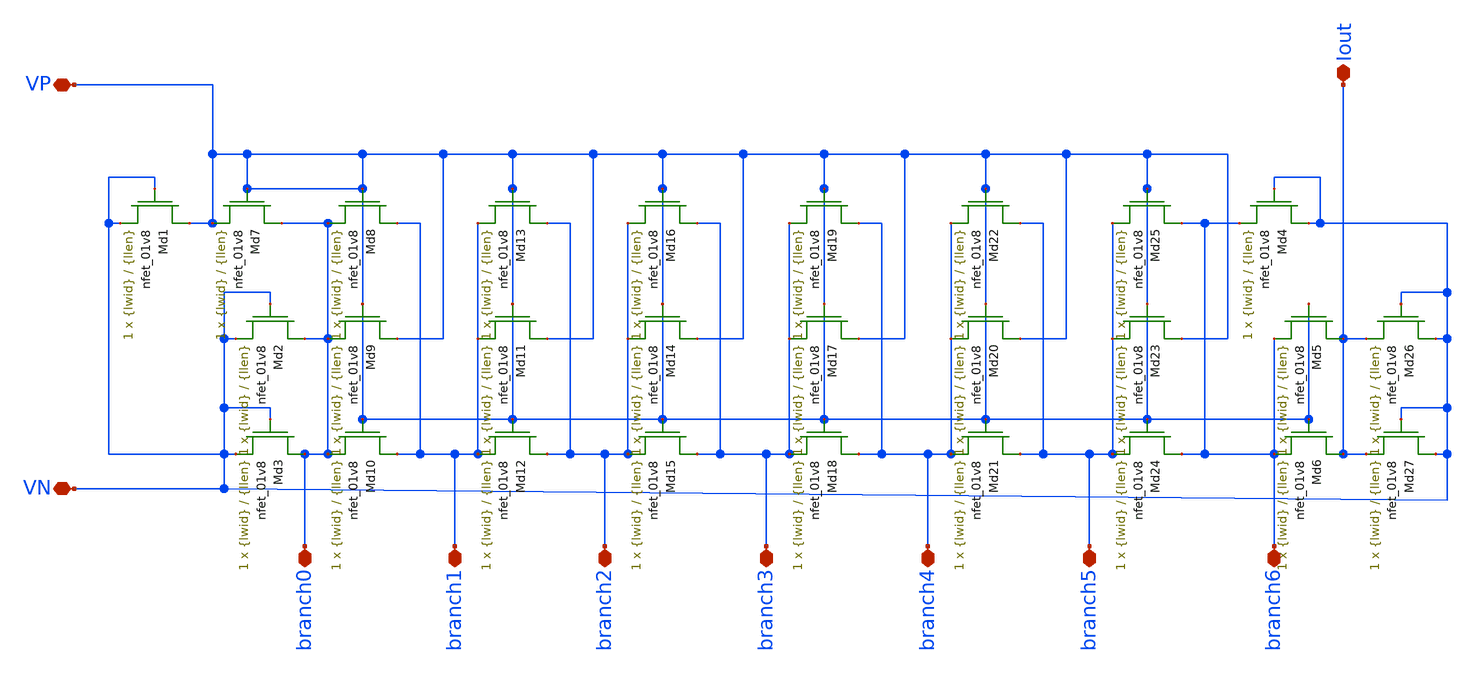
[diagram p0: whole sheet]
** sch_path: design-files/improved/dacladder-m2.sch
**.subckt dacladder-m2 branch0 branch1 branch2 branch3 branch4 branch5 branch6 Iout VN VP
*.iopin branch0
*.iopin branch1
*.iopin branch2
*.iopin branch3
*.iopin branch4
*.iopin branch5
*.iopin branch6
*.iopin Iout
*.iopin VN
*.iopin VP
XMd1 VP VN VN GND sky130_fd_pr__nfet_01v8 L={llen} W={lwid} nf=1 ad='int((nf+1)/2) * W/nf * 0.29' as='int((nf+2)/2) * W/nf * 0.29'
+ pd='2*int((nf+1)/2) * (W/nf + 0.29)' ps='2*int((nf+2)/2) * (W/nf + 0.29)' nrd='0.29 / W' nrs='0.29 / W'
+ sa=0 sb=0 sd=0 mult=1 m=1
XMd7 branch0 VP VP GND sky130_fd_pr__nfet_01v8 L={llen} W={lwid} nf=1 ad='int((nf+1)/2) * W/nf * 0.29'
+ as='int((nf+2)/2) * W/nf * 0.29' pd='2*int((nf+1)/2) * (W/nf + 0.29)' ps='2*int((nf+2)/2) * (W/nf + 0.29)'
+ nrd='0.29 / W' nrs='0.29 / W' sa=0 sb=0 sd=0 mult=1 m=1
XMd8 branch1 VP branch0 GND sky130_fd_pr__nfet_01v8 L={llen} W={lwid} nf=1 ad='int((nf+1)/2) * W/nf * 0.29'
+ as='int((nf+2)/2) * W/nf * 0.29' pd='2*int((nf+1)/2) * (W/nf + 0.29)' ps='2*int((nf+2)/2) * (W/nf + 0.29)'
+ nrd='0.29 / W' nrs='0.29 / W' sa=0 sb=0 sd=0 mult=1 m=1
XMd2 branch0 VN VN GND sky130_fd_pr__nfet_01v8 L={llen} W={lwid} nf=1 ad='int((nf+1)/2) * W/nf * 0.29'
+ as='int((nf+2)/2) * W/nf * 0.29' pd='2*int((nf+1)/2) * (W/nf + 0.29)' ps='2*int((nf+2)/2) * (W/nf + 0.29)'
+ nrd='0.29 / W' nrs='0.29 / W' sa=0 sb=0 sd=0 mult=1 m=1
XMd9 VP VP branch0 GND sky130_fd_pr__nfet_01v8 L={llen} W={lwid} nf=1 ad='int((nf+1)/2) * W/nf * 0.29'
+ as='int((nf+2)/2) * W/nf * 0.29' pd='2*int((nf+1)/2) * (W/nf + 0.29)' ps='2*int((nf+2)/2) * (W/nf + 0.29)'
+ nrd='0.29 / W' nrs='0.29 / W' sa=0 sb=0 sd=0 mult=1 m=1
XMd3 branch0 VN VN GND sky130_fd_pr__nfet_01v8 L={llen} W={lwid} nf=1 ad='int((nf+1)/2) * W/nf * 0.29'
+ as='int((nf+2)/2) * W/nf * 0.29' pd='2*int((nf+1)/2) * (W/nf + 0.29)' ps='2*int((nf+2)/2) * (W/nf + 0.29)'
+ nrd='0.29 / W' nrs='0.29 / W' sa=0 sb=0 sd=0 mult=1 m=1
XMd10 branch1 VP branch0 GND sky130_fd_pr__nfet_01v8 L={llen} W={lwid} nf=1 ad='int((nf+1)/2) * W/nf * 0.29'
+ as='int((nf+2)/2) * W/nf * 0.29' pd='2*int((nf+1)/2) * (W/nf + 0.29)' ps='2*int((nf+2)/2) * (W/nf + 0.29)'
+ nrd='0.29 / W' nrs='0.29 / W' sa=0 sb=0 sd=0 mult=1 m=1
XMd11 VP VP branch1 GND sky130_fd_pr__nfet_01v8 L={llen} W={lwid} nf=1 ad='int((nf+1)/2) * W/nf * 0.29'
+ as='int((nf+2)/2) * W/nf * 0.29' pd='2*int((nf+1)/2) * (W/nf + 0.29)' ps='2*int((nf+2)/2) * (W/nf + 0.29)'
+ nrd='0.29 / W' nrs='0.29 / W' sa=0 sb=0 sd=0 mult=1 m=1
XMd12 branch2 VP branch1 GND sky130_fd_pr__nfet_01v8 L={llen} W={lwid} nf=1 ad='int((nf+1)/2) * W/nf * 0.29'
+ as='int((nf+2)/2) * W/nf * 0.29' pd='2*int((nf+1)/2) * (W/nf + 0.29)' ps='2*int((nf+2)/2) * (W/nf + 0.29)'
+ nrd='0.29 / W' nrs='0.29 / W' sa=0 sb=0 sd=0 mult=1 m=1
XMd13 branch2 VP branch1 GND sky130_fd_pr__nfet_01v8 L={llen} W={lwid} nf=1 ad='int((nf+1)/2) * W/nf * 0.29'
+ as='int((nf+2)/2) * W/nf * 0.29' pd='2*int((nf+1)/2) * (W/nf + 0.29)' ps='2*int((nf+2)/2) * (W/nf + 0.29)'
+ nrd='0.29 / W' nrs='0.29 / W' sa=0 sb=0 sd=0 mult=1 m=1
XMd14 VP VP branch2 GND sky130_fd_pr__nfet_01v8 L={llen} W={lwid} nf=1 ad='int((nf+1)/2) * W/nf * 0.29'
+ as='int((nf+2)/2) * W/nf * 0.29' pd='2*int((nf+1)/2) * (W/nf + 0.29)' ps='2*int((nf+2)/2) * (W/nf + 0.29)'
+ nrd='0.29 / W' nrs='0.29 / W' sa=0 sb=0 sd=0 mult=1 m=1
XMd15 branch3 VP branch2 GND sky130_fd_pr__nfet_01v8 L={llen} W={lwid} nf=1 ad='int((nf+1)/2) * W/nf * 0.29'
+ as='int((nf+2)/2) * W/nf * 0.29' pd='2*int((nf+1)/2) * (W/nf + 0.29)' ps='2*int((nf+2)/2) * (W/nf + 0.29)'
+ nrd='0.29 / W' nrs='0.29 / W' sa=0 sb=0 sd=0 mult=1 m=1
XMd16 branch3 VP branch2 GND sky130_fd_pr__nfet_01v8 L={llen} W={lwid} nf=1 ad='int((nf+1)/2) * W/nf * 0.29'
+ as='int((nf+2)/2) * W/nf * 0.29' pd='2*int((nf+1)/2) * (W/nf + 0.29)' ps='2*int((nf+2)/2) * (W/nf + 0.29)'
+ nrd='0.29 / W' nrs='0.29 / W' sa=0 sb=0 sd=0 mult=1 m=1
XMd17 VP VP branch3 GND sky130_fd_pr__nfet_01v8 L={llen} W={lwid} nf=1 ad='int((nf+1)/2) * W/nf * 0.29'
+ as='int((nf+2)/2) * W/nf * 0.29' pd='2*int((nf+1)/2) * (W/nf + 0.29)' ps='2*int((nf+2)/2) * (W/nf + 0.29)'
+ nrd='0.29 / W' nrs='0.29 / W' sa=0 sb=0 sd=0 mult=1 m=1
XMd18 branch4 VP branch3 GND sky130_fd_pr__nfet_01v8 L={llen} W={lwid} nf=1 ad='int((nf+1)/2) * W/nf * 0.29'
+ as='int((nf+2)/2) * W/nf * 0.29' pd='2*int((nf+1)/2) * (W/nf + 0.29)' ps='2*int((nf+2)/2) * (W/nf + 0.29)'
+ nrd='0.29 / W' nrs='0.29 / W' sa=0 sb=0 sd=0 mult=1 m=1
XMd19 branch4 VP branch3 GND sky130_fd_pr__nfet_01v8 L={llen} W={lwid} nf=1 ad='int((nf+1)/2) * W/nf * 0.29'
+ as='int((nf+2)/2) * W/nf * 0.29' pd='2*int((nf+1)/2) * (W/nf + 0.29)' ps='2*int((nf+2)/2) * (W/nf + 0.29)'
+ nrd='0.29 / W' nrs='0.29 / W' sa=0 sb=0 sd=0 mult=1 m=1
XMd20 VP VP branch4 GND sky130_fd_pr__nfet_01v8 L={llen} W={lwid} nf=1 ad='int((nf+1)/2) * W/nf * 0.29'
+ as='int((nf+2)/2) * W/nf * 0.29' pd='2*int((nf+1)/2) * (W/nf + 0.29)' ps='2*int((nf+2)/2) * (W/nf + 0.29)'
+ nrd='0.29 / W' nrs='0.29 / W' sa=0 sb=0 sd=0 mult=1 m=1
XMd21 branch5 VP branch4 GND sky130_fd_pr__nfet_01v8 L={llen} W={lwid} nf=1 ad='int((nf+1)/2) * W/nf * 0.29'
+ as='int((nf+2)/2) * W/nf * 0.29' pd='2*int((nf+1)/2) * (W/nf + 0.29)' ps='2*int((nf+2)/2) * (W/nf + 0.29)'
+ nrd='0.29 / W' nrs='0.29 / W' sa=0 sb=0 sd=0 mult=1 m=1
XMd22 branch5 VP branch4 GND sky130_fd_pr__nfet_01v8 L={llen} W={lwid} nf=1 ad='int((nf+1)/2) * W/nf * 0.29'
+ as='int((nf+2)/2) * W/nf * 0.29' pd='2*int((nf+1)/2) * (W/nf + 0.29)' ps='2*int((nf+2)/2) * (W/nf + 0.29)'
+ nrd='0.29 / W' nrs='0.29 / W' sa=0 sb=0 sd=0 mult=1 m=1
XMd23 VP VP branch5 GND sky130_fd_pr__nfet_01v8 L={llen} W={lwid} nf=1 ad='int((nf+1)/2) * W/nf * 0.29'
+ as='int((nf+2)/2) * W/nf * 0.29' pd='2*int((nf+1)/2) * (W/nf + 0.29)' ps='2*int((nf+2)/2) * (W/nf + 0.29)'
+ nrd='0.29 / W' nrs='0.29 / W' sa=0 sb=0 sd=0 mult=1 m=1
XMd24 branch6 VP branch5 GND sky130_fd_pr__nfet_01v8 L={llen} W={lwid} nf=1 ad='int((nf+1)/2) * W/nf * 0.29'
+ as='int((nf+2)/2) * W/nf * 0.29' pd='2*int((nf+1)/2) * (W/nf + 0.29)' ps='2*int((nf+2)/2) * (W/nf + 0.29)'
+ nrd='0.29 / W' nrs='0.29 / W' sa=0 sb=0 sd=0 mult=1 m=1
XMd25 branch6 VP branch5 GND sky130_fd_pr__nfet_01v8 L={llen} W={lwid} nf=1 ad='int((nf+1)/2) * W/nf * 0.29'
+ as='int((nf+2)/2) * W/nf * 0.29' pd='2*int((nf+1)/2) * (W/nf + 0.29)' ps='2*int((nf+2)/2) * (W/nf + 0.29)'
+ nrd='0.29 / W' nrs='0.29 / W' sa=0 sb=0 sd=0 mult=1 m=1
XMd4 VN VN branch6 GND sky130_fd_pr__nfet_01v8 L={llen} W={lwid} nf=1 ad='int((nf+1)/2) * W/nf * 0.29'
+ as='int((nf+2)/2) * W/nf * 0.29' pd='2*int((nf+1)/2) * (W/nf + 0.29)' ps='2*int((nf+2)/2) * (W/nf + 0.29)'
+ nrd='0.29 / W' nrs='0.29 / W' sa=0 sb=0 sd=0 mult=1 m=1
XMd5 Iout VP branch6 GND sky130_fd_pr__nfet_01v8 L={llen} W={lwid} nf=1 ad='int((nf+1)/2) * W/nf * 0.29'
+ as='int((nf+2)/2) * W/nf * 0.29' pd='2*int((nf+1)/2) * (W/nf + 0.29)' ps='2*int((nf+2)/2) * (W/nf + 0.29)'
+ nrd='0.29 / W' nrs='0.29 / W' sa=0 sb=0 sd=0 mult=1 m=1
XMd26 VN VN Iout GND sky130_fd_pr__nfet_01v8 L={llen} W={lwid} nf=1 ad='int((nf+1)/2) * W/nf * 0.29'
+ as='int((nf+2)/2) * W/nf * 0.29' pd='2*int((nf+1)/2) * (W/nf + 0.29)' ps='2*int((nf+2)/2) * (W/nf + 0.29)'
+ nrd='0.29 / W' nrs='0.29 / W' sa=0 sb=0 sd=0 mult=1 m=1
XMd6 Iout VP branch6 GND sky130_fd_pr__nfet_01v8 L={llen} W={lwid} nf=1 ad='int((nf+1)/2) * W/nf * 0.29'
+ as='int((nf+2)/2) * W/nf * 0.29' pd='2*int((nf+1)/2) * (W/nf + 0.29)' ps='2*int((nf+2)/2) * (W/nf + 0.29)'
+ nrd='0.29 / W' nrs='0.29 / W' sa=0 sb=0 sd=0 mult=1 m=1
XMd27 VN VN Iout GND sky130_fd_pr__nfet_01v8 L={llen} W={lwid} nf=1 ad='int((nf+1)/2) * W/nf * 0.29'
+ as='int((nf+2)/2) * W/nf * 0.29' pd='2*int((nf+1)/2) * (W/nf + 0.29)' ps='2*int((nf+2)/2) * (W/nf + 0.29)'
+ nrd='0.29 / W' nrs='0.29 / W' sa=0 sb=0 sd=0 mult=1 m=1
**.ends
.end
